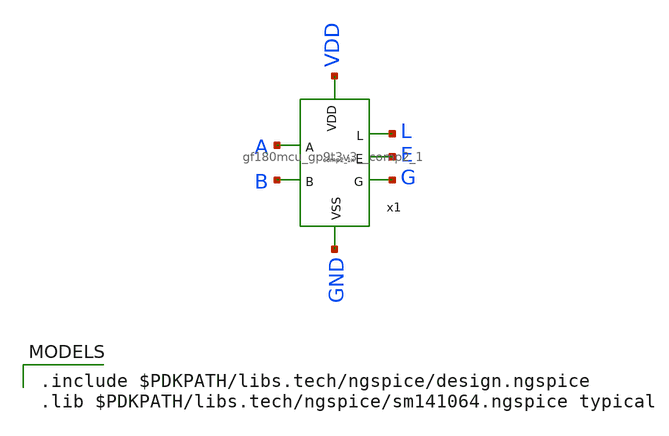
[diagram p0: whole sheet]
** sch_path: cells/comp2/schematic/testbench/tb_comp2_1x.sch
**.subckt tb_comp2_1x
x1 VDD L A E G B GND gf180mcu_gp9t3v3__comp2_1
**** begin user architecture code

.include $PDKPATH/libs.tech/ngspice/design.ngspice
.lib $PDKPATH/libs.tech/ngspice/sm141064.ngspice typical


* Stimuli
* VPOWER VDD gnd DC 3.3
* V_A A gnd PWL(0 0 {10n-10p} 0 {10n+10p} 3.3 {20n-10p} 3.3 {20n+10p} 0 {30n-10p} 0 {30n+10p} 3.3 40n
*+ 3.3)
* V_B B gnd PWL(0 0 {20n-10p} 0 {20n+10p} 3.3 40n 3.3)

* Simulation
* .tran 1p 40n
* .control
* run
* save all
* plot G E+4 L+8 B+12 A+16
* .endc
* .GLOBAL gnd
* .end


* Define parameters
.GLOBAL gnd
.temp 25
.param vdd = 3.3V
.param slew_in = 10p
.param cload = 1f
.param vh = {vdd/2}
.param v_10 = {vdd*0.1}
.param v_90 = {vdd*0.9}
* For printing purposes
.csparam outload = {1*cload}
.csparam slewin = {1*slew_in}

* ---- STIMULIS ----
* Power
VVDD VDD gnd DC {vdd}

* Change stimuli here!
VA A gnd PULSE({vdd} 0 1n {slew_in} {slew_in} 2n 4n)
VB B gnd DC 0

* Load capacitance & additional loads
VmeasL L L_load 0
CLL L_load gnd {cload}
VmeasE E E_load 0
CLE E_load gnd {cload}
VmeasG G G_load 0
CLG G_load gnd {cload}

********************************************************************************
* Analysis Statements
********************************************************************************
.OPTIONS SAVE CURRENTS
.tran 1p 10n
* ---- DYNAMIC ENERGY MEASUREMENT (Pin) ----
* Measuring energy that sent to the load capacitor for each pin
* Dynamic power will be positive when LH and negative when HL
.MEASURE TRAN curr_L_uJ INTEG I(VmeasL) from=0 to=10n
.MEASURE TRAN energy_L_uJ param='curr_L_uJ * vdd'
.MEASURE TRAN curr_E_uJ INTEG I(VmeasE) from=0 to=10n
.MEASURE TRAN energy_E_uJ param='curr_E_uJ * vdd'
.MEASURE TRAN curr_G_uJ INTEG I(VmeasG) from=0 to=10n
.MEASURE TRAN energy_G_uJ param='curr_G_uJ * vdd'

* Total energy of VDD measurement
.measure tran curr_TOTAL_uJ INTEG I(vvdd) from=0 to=10n
.measure tran energy_TOTAL_uJ param='curr_TOTAL_uJ * (-1) * vdd'

********************************************************************************
* Simulation Control Block
********************************************************************************
.control
    run
.endc
.end


* Copy and paste this line to code "ANALYSIS"
* Stimuli: A(HL) and B
* VA A gnd PULSE({vdd} 0 1n {slew_in} {slew_in} 2n 4n)
* VB B gnd DC {vdd}

* Stimuli: A(HL) and !B
* VA A gnd PULSE({vdd} 0 1n {slew_in} {slew_in} 2n 4n)
* VB B gnd DC 0

* Stimuli: A(LH) and B
* VA A gnd PULSE(0 {vdd} 1n {slew_in} {slew_in} 2n 4n)
* VB B gnd DC {vdd}

* Stimuli: A(LH) and !B
* VA A gnd PULSE(0 {vdd} 1n {slew_in} {slew_in} 2n 4n)
* VB B gnd DC 0

* Stimuli: B(HL) and A
* VA A gnd DC {vdd}
* VB B gnd PULSE({vdd} 0 1n {slew_in} {slew_in} 2n 4n)

* Stimuli: B(HL) and !A
* VA A gnd DC 0
* VB B gnd PULSE({vdd} 0 1n {slew_in} {slew_in} 2n 4n)

* Stimuli: B(LH) and A
* VA A gnd DC {vdd}
* VB B gnd PULSE(0 {vdd} 1n {slew_in} {slew_in} 2n 4n)

* Stimuli: B(LH) and !A
* VA A gnd DC 0
* VB B gnd PULSE(0 {vdd} 1n {slew_in} {slew_in} 2n 4n)

* .OPTIONS SAVE CURRENTS
* .tran 1p 10n

* --- Delay and Slew Measurements ---
* Stimuli: A(HL) and B -> L(LH) & E(HL)
* Delay and Rise Time of L(LH)
* .MEASURE TRAN delay_AHL_B_L TRIG V(A) VAL={vh} FALL=1 TARG V(L) VAL={vh} RISE=1
* .MEASURE TRAN rise_AHL_B_L TRIG V(L) VAL={v_10} RISE=1 TARG V(L) VAL={v_90} RISE=1
* Delay and Fall Time of E(HL)
* .MEASURE TRAN delay_AHL_B_E TRIG V(A) VAL={vh} FALL=1 TARG V(E) VAL={vh} FALL=1
* .MEASURE TRAN fall_AHL_B_E TRIG V(E) VAL={v_90} FALL=1 TARG V(E) VAL={v_10} FALL=1

* Stimuli: A(HL) and !B -> E(LH) & G(HL)
* Delay and Rise Time of E(LH)
* .MEASURE TRAN delay_AHL_noB_E TRIG V(A) VAL={vh} FALL=1 TARG V(E) VAL={vh} RISE=1
* .MEASURE TRAN rise_AHL_noB_E TRIG V(E) VAL={v_10} RISE=1 TARG V(E) VAL={v_90} RISE=1
* Delay and Fall Time of G(HL)
* .MEASURE TRAN delay_AHL_noB_G TRIG V(A) VAL={vh} FALL=1 TARG V(G) VAL={vh} FALL=1
* .MEASURE TRAN fall_AHL_noB_G TRIG V(G) VAL={v_90} FALL=1 TARG V(G) VAL={v_10} FALL=1

* Stimuli: A(LH) and B -> L(HL) & E(LH)
* Delay and Fall Time of L(HL)
* .MEASURE TRAN delay_ALH_B_L TRIG V(A) VAL={vh} RISE=1 TARG V(L) VAL={vh} FALL=1
* .MEASURE TRAN fall_ALH_B_L TRIG V(L) VAL={v_90} FALL=1 TARG V(L) VAL={v_10} FALL=1
* Delay and Rise Time of E(LH)
* .MEASURE TRAN delay_ALH_B_E TRIG V(A) VAL={vh} RISE=1 TARG V(E) VAL={vh} RISE=1
* .MEASURE TRAN rise_ALH_B_E TRIG V(E) VAL={v_10} RISE=1 TARG V(E) VAL={v_90} RISE=1

* Stimuli: A(LH) and !B -> E(HL) & G(LH)
* Delay and Fall Time of E(HL)
* .MEASURE TRAN delay_ALH_noB_E TRIG V(A) VAL={vh} RISE=1 TARG V(E) VAL={vh} FALL=1
* .MEASURE TRAN fall_ALH_noB_E TRIG V(E) VAL={v_90} FALL=1 TARG V(E) VAL={v_10} FALL=1
* Delay and Rise Time of G(LH)
* .MEASURE TRAN delay_ALH_noB_G TRIG V(A) VAL={vh} RISE=1 TARG V(G) VAL={vh} RISE=1
* .MEASURE TRAN rise_ALH_noB_G TRIG V(G) VAL={v_10} RISE=1 TARG V(G) VAL={v_90} RISE=1

* Stimuli: B(HL) and A -> E(HL) & G(LH)
* Delay and Fall Time of E(HL)
* .MEASURE TRAN delay_BHL_A_E TRIG V(B) VAL={vh} FALL=1 TARG V(E) VAL={vh} FALL=1
* .MEASURE TRAN fall_BHL_A_E TRIG V(E) VAL={v_90} FALL=1 TARG V(E) VAL={v_10} FALL=1
* Delay and Rise Time of G(LH)
* .MEASURE TRAN delay_BHL_A_G TRIG V(B) VAL={vh} FALL=1 TARG V(G) VAL={vh} RISE=1
* .MEASURE TRAN rise_BHL_A_G TRIG V(G) VAL={v_10} RISE=1 TARG V(G) VAL={v_90} RISE=1

* Stimuli: B(HL) and !A -> L(HL) & E(LH)
* Delay and Fall Time of L(HL)
* .MEASURE TRAN delay_BHL_noA_L TRIG V(B) VAL={vh} FALL=1 TARG V(L) VAL={vh} FALL=1
* .MEASURE TRAN fall_BHL_noA_L TRIG V(L) VAL={v_90} FALL=1 TARG V(L) VAL={v_10} FALL=1
* Delay and Rise Time of E(LH)
* .MEASURE TRAN delay_BHL_noA_E TRIG V(B) VAL={vh} FALL=1 TARG V(E) VAL={vh} RISE=1
* .MEASURE TRAN rise_BHL_noA_E TRIG V(E) VAL={v_10} RISE=1 TARG V(E) VAL={v_90} RISE=1

* Stimuli: B(LH) and A -> E(LH) & G(HL)
* Delay and Rise Time of E(LH)
* .MEASURE TRAN delay_BLH_A_E TRIG V(B) VAL={vh} RISE=1 TARG V(E) VAL={vh} RISE=1
* .MEASURE TRAN rise_BLH_A_E TRIG V(E) VAL={v_10} RISE=1 TARG V(E) VAL={v_90} RISE=1
* Delay and Fall Time of G(HL)
* .MEASURE TRAN delay_BLH_A_G TRIG V(B) VAL={vh} RISE=1 TARG V(G) VAL={vh} FALL=1
* .MEASURE TRAN fall_BLH_A_G TRIG V(G) VAL={v_90} FALL=1 TARG V(G) VAL={v_10} FALL=1

* Stimuli: B(LH) and !A -> L(LH) & E(HL)
* Delay and Rise Time of L(LH)
* .MEASURE TRAN delay_BLH_noA_L TRIG V(B) VAL={vh} RISE=1 TARG V(L) VAL={vh} RISE=1
* .MEASURE TRAN rise_BLH_noA_L TRIG V(L) VAL={v_10} RISE=1 TARG V(L) VAL={v_90} RISE=1
* Delay and Fall Time of E(HL)
* .MEASURE TRAN delay_BLH_noA_E TRIG V(B) VAL={vh} RISE=1 TARG V(E) VAL={vh} FALL=1
* .MEASURE TRAN fall_BLH_noA_E TRIG V(E) VAL={v_90} FALL=1 TARG V(E) VAL={v_10} FALL=1

* .control
	* Delay and Output Transition Time Analysis
	* echo "========================================================================"
    	* echo "1. Delay and Output Transition Time Analysis"
	* echo -n "   Input Slew = "
	* echo $&slewin
	* echo -n "   Output Load = "
	* echo $&outload
    	* echo "------------------------------------------------------------------------"

	* Stimuli 1: A(HL) & B -> L(LH) & E(HL)
	* alter @VA[pulse] = [ {vdd} 0 1n {slew_in} {slew_in} 2n 4n ]
	* alter @VB[dc] = {vdd}
	* run
	* echo -n "  > Delay A(HL)->L(LH): "; print delay_AHL_B_L
	* echo -n "  > Slew L(LH):     "; print rise_AHL_B_L
	* echo -n "  > Delay A(HL)->E(HL): "; print delay_AHL_B_E
	* echo -n "  > Slew E(HL):     "; print fall_AHL_B_E

	* Stimuli 2: A(HL) & !B -> E(LH) & G(HL)
	* alter @VB[dc] = 0
	* run
	* echo -n "  > Delay A(HL)->E(LH): "; print delay_AHL_noB_E
	* echo -n "  > Slew E(LH):     "; print rise_AHL_noB_E
	* echo -n "  > Delay A(HL)->G(HL): "; print delay_AHL_noB_G
	* echo -n "  > Slew G(HL):     "; print fall_AHL_noB_G

	* Stimuli 3: A(LH) & B -> L(HL) & E(LH)
	* alter @VA[pulse] = [ 0 {vdd} 1n {slew_in} {slew_in} 2n 4n ]
	* alter @VB[dc] = {vdd}
	* run
	* echo -n "  > Delay A(LH)->L(HL): "; print delay_ALH_B_L
	* echo -n "  > Slew L(HL):     "; print fall_ALH_B_L
	* echo -n "  > Delay A(LH)->E(LH): "; print delay_ALH_B_E
	* echo -n "  > Slew E(LH):     "; print rise_ALH_B_E

	* Stimuli 4: A(LH) & !B -> E(HL) & G(LH)
	* alter @VB[dc] = 0
	* run
	* echo -n "  > Delay A(LH)->E(HL): "; print delay_ALH_noB_E
	* echo -n "  > Slew E(HL):     "; print fall_ALH_noB_E
	* echo -n "  > Delay A(LH)->G(LH): "; print delay_ALH_noB_G
	* echo -n "  > Slew G(LH):     "; print rise_ALH_noB_G

	* Stimuli 5: B(HL) & A -> E(HL) & G(LH)
	* alter @VA[dc] = {vdd}
	* alter @VB[pulse] = [ {vdd} 0 1n {slew_in} {slew_in} 2n 4n ]
	* run
	* echo -n "  -> Delay B(HL)->E(HL): "; print delay_BHL_A_E
	* echo -n "  -> Slew E(HL):     "; print fall_BHL_A_E
	* echo -n "  -> Delay B(HL)->G(LH): "; print delay_BHL_A_G
	* echo -n "  -> Slew G(LH):     "; print rise_BHL_A_G

	* Stimuli 6: B(HL) & !A -> L(HL) & E(LH)
	* alter @VA[dc] = 0
	* run
	* echo -n "  -> Delay B(HL)->L(HL): "; print delay_BHL_noA_L
	* echo -n "  -> Slew L(HL):     "; print fall_BHL_noA_L
	* echo -n "  -> Delay B(HL)->E(LH): "; print delay_BHL_noA_E
	* echo -n "  -> Slew E(LH):     "; print rise_BHL_noA_E

	* Stimuli 7: B(LH) & A -> E(LH) & G(HL)
	* alter @VA[dc] = {vdd}
	* alter @VB[pulse] = [ 0 {vdd} 1n {slew_in} {slew_in} 2n 4n ]
	* run
	* echo -n "  -> Delay B(LH)->E(LH): "; print delay_BLH_A_E
	* echo -n "  -> Slew E(LH):     "; print rise_BLH_A_E
	* echo -n "  -> Delay B(LH)->G(HL): "; print delay_BLH_A_G
	* echo -n "  -> Slew G(HL):     "; print fall_BLH_A_G

	* Stimuli 8: B(LH) & !A -> L(LH) & E(HL)
	* alter @VA[dc] = 0
	* run
	* echo -n "  -> Delay B(LH)->L(LH): "; print delay_BLH_noA_L
	* echo -n "  -> Slew L(LH):     "; print rise_BLH_noA_L
	* echo -n "  -> Delay B(LH)->E(HL): "; print delay_BLH_noA_E
	* echo -n "  -> Slew E(HL):     "; print fall_BLH_noA_E


* STIMULI
* !A & !B
* VA A gnd DC 0
* VB B gnd DC 0

* !A & B
* VA A gnd DC 0
* VB B gnd DC {vdd}

* A & !B
* VA A gnd DC {vdd}
* VB B gnd DC 0

* A & B
* VA A gnd DC {vdd}
* VB B gnd DC {vdd}

* .OP

* .control
	* run
	* let leakage_current = -I(VVDD)
	* let leak_watt = {vdd}*leakage_current
	* print leak_watt
	* save all
* .endc
* .end


* Stimuli: A(HL) and B
* VA A gnd PULSE({vdd} 0 1n {slew_in} {slew_in} 2n 4n)
* VB B gnd DC {vdd}

* Stimuli: A(HL) and !B
* VA A gnd PULSE({vdd} 0 1n {slew_in} {slew_in} 2n 4n)
* VB B gnd DC 0

* Stimuli: A(LH) and B
* VA A gnd PULSE(0 {vdd} 1n {slew_in} {slew_in} 2n 4n)
* VB B gnd DC {vdd}

* Stimuli: A(LH) and !B
* VA A gnd PULSE(0 {vdd} 1n {slew_in} {slew_in} 2n 4n)
* VB B gnd DC 0

* Stimuli: B(HL) and A
* VA A gnd DC {vdd}
* VB B gnd PULSE({vdd} 0 1n {slew_in} {slew_in} 2n 4n)

* Stimuli: B(HL) and !A
* VA A gnd DC 0
* VB B gnd PULSE({vdd} 0 1n {slew_in} {slew_in} 2n 4n)

* Stimuli: B(LH) and A
* VA A gnd DC {vdd}
* VB B gnd PULSE(0 {vdd} 1n {slew_in} {slew_in} 2n 4n)

* Stimuli: B(LH) and !A
* VA A gnd DC 0
* VB B gnd PULSE(0 {vdd} 1n {slew_in} {slew_in} 2n 4n)

* VmeasL L L_load 0
* CLL L_load gnd {cload}
* VmeasE E E_load 0
* CLE E_load gnd {cload}
* VmeasG G G_load 0
* CLG G_load gnd {cload}

* .OPTIONS SAVE CURRENTS
* .tran 1p 10n

* ---- DYNAMIC ENERGY MEASUREMENT (Pin) ----
* Measuring energy that sent to the load capacitor for each pin
* Dynamic power will be positive when LH and negative when HL
* .MEASURE TRAN curr_L_uJ INTEG I(VmeasL) from=0 to=10n
* .MEASURE TRAN energy_L_uJ param='curr_L_uJ * vdd'
* .MEASURE TRAN curr_E_uJ INTEG I(VmeasE) from=0 to=10n
* .MEASURE TRAN energy_E_uJ param='curr_E_uJ * vdd'
* .MEASURE TRAN curr_G_uJ INTEG I(VmeasG) from=0 to=10n
* .MEASURE TRAN energy_G_uJ param='curr_G_uJ * vdd'

* Total energy of VDD measurement
* .measure tran curr_TOTAL_uJ INTEG I(vvdd) from=0 to=10n
* .measure tran energy_TOTAL_uJ param='curr_TOTAL_uJ * (-1) * vdd'
    * run

    * echo "========================================================================"
    * echo "          Dynamic Energy Analysis Results (uW/MHz atau uJ/cycle)"
    * echo "========================================================================"
    * echo "CATATAN: Nilai energi yang mendekati nol berarti tidak ada transisi"
    * echo "         pada pin output tersebut untuk stimulus yang dipilih."
    * echo "------------------------------------------------------------------------"

    * print energy_L_uJ
    * print energy_E_uJ
    * print energy_G_uJ

    * echo "------------------------------------------------------------------------"
    * print energy_TOTAL_uJ
    * echo "========================================================================"

**** end user architecture code
**.ends
.end
